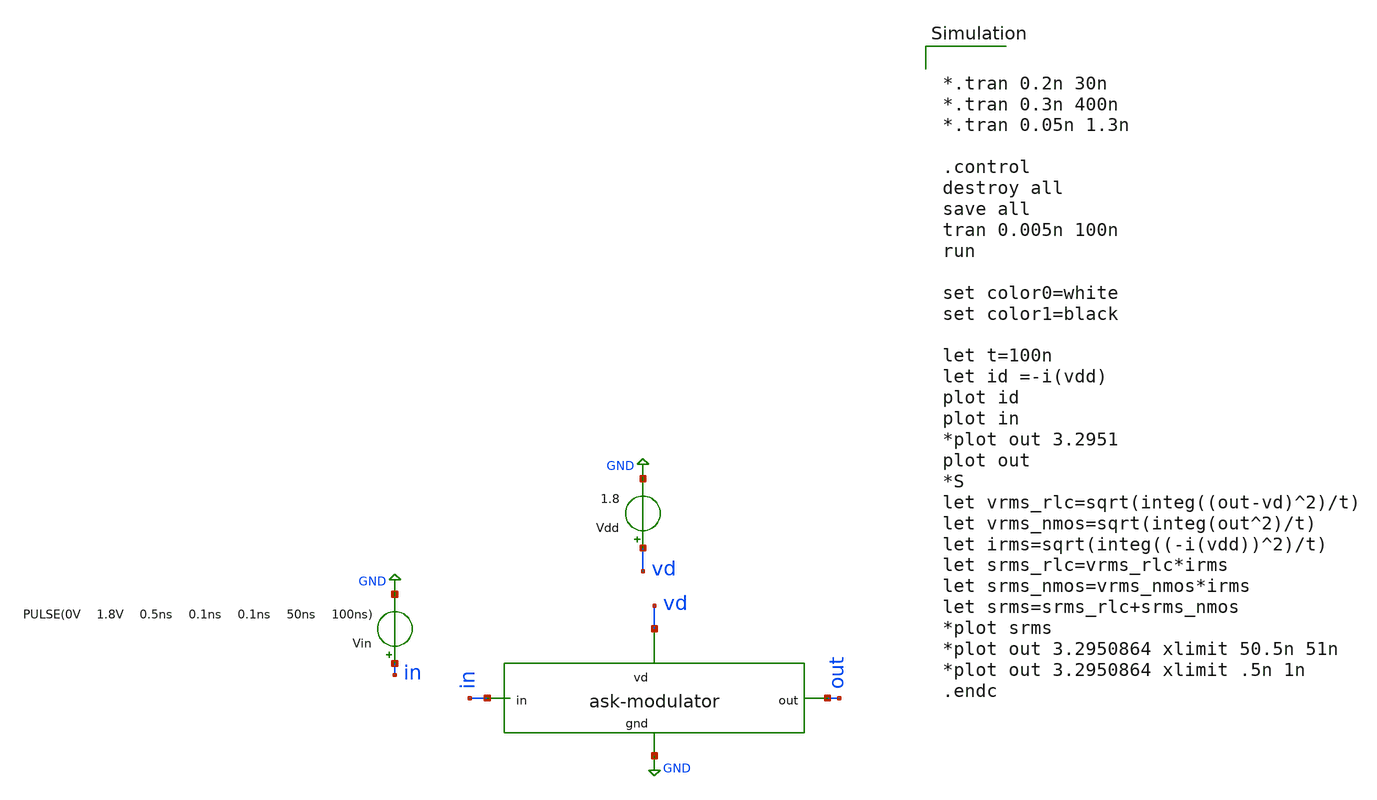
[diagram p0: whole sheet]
** sch_path: ask_modulator/xschem/ask-modulator_tb-tran.sch
**.subckt ask-modulator_tb-tran
Vdd vd GND 1.8
Vin in GND PULSE(0V 1.8V 0.5ns 0.1ns 0.1ns 50ns 100ns)
x1 vd out in GND ask-modulator
**** begin user architecture code


*.tran 0.2n 30n
*.tran 0.3n 400n
*.tran 0.05n 1.3n

.control
destroy all
save all
tran 0.005n 100n
run

set color0=white
set color1=black

let t=100n
let id =-i(vdd)
plot id
plot in
*plot out 3.2951
plot out
*S
let vrms_rlc=sqrt(integ((out-vd)^2)/t)
let vrms_nmos=sqrt(integ(out^2)/t)
let irms=sqrt(integ((-i(vdd))^2)/t)
let srms_rlc=vrms_rlc*irms
let srms_nmos=vrms_nmos*irms
let srms=srms_rlc+srms_nmos
*plot srms
*plot out 3.2950864 xlimit 50.5n 51n
*plot out 3.2950864 xlimit .5n 1n
.endc

 .lib $::SKYWATER_MODELS/sky130.lib.spice tt
.include $::SKYWATER_STDCELLS/sky130_fd_sc_hd.spice

**** end user architecture code
**.ends
.GLOBAL GND
.end
